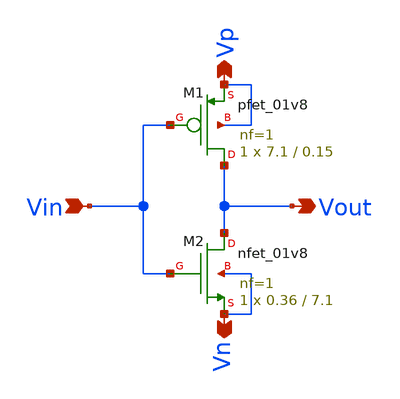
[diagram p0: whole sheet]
** sch_path: xschem/Vth_sch/Symbol/Inverter-th11.sch
**.subckt Inverter-th11 Vin Vout Vn Vp
*.ipin Vin
*.opin Vout
*.opin Vn
*.opin Vp
XM1 Vout Vin Vp Vp sky130_fd_pr__pfet_01v8 L=0.15 W=7.1 nf=1 ad='int((nf+1)/2) * W/nf * 0.29' as='int((nf+2)/2) * W/nf * 0.29'
+ pd='2*int((nf+1)/2) * (W/nf + 0.29)' ps='2*int((nf+2)/2) * (W/nf + 0.29)' nrd='0.29 / W' nrs='0.29 / W'
+ sa=0 sb=0 sd=0 mult=1 m=1
XM2 Vout Vin Vn Vn sky130_fd_pr__nfet_01v8 L=7.1 W=0.36 nf=1 ad='int((nf+1)/2) * W/nf * 0.29' as='int((nf+2)/2) * W/nf * 0.29'
+ pd='2*int((nf+1)/2) * (W/nf + 0.29)' ps='2*int((nf+2)/2) * (W/nf + 0.29)' nrd='0.29 / W' nrs='0.29 / W'
+ sa=0 sb=0 sd=0 mult=1 m=1
**.ends
.end
